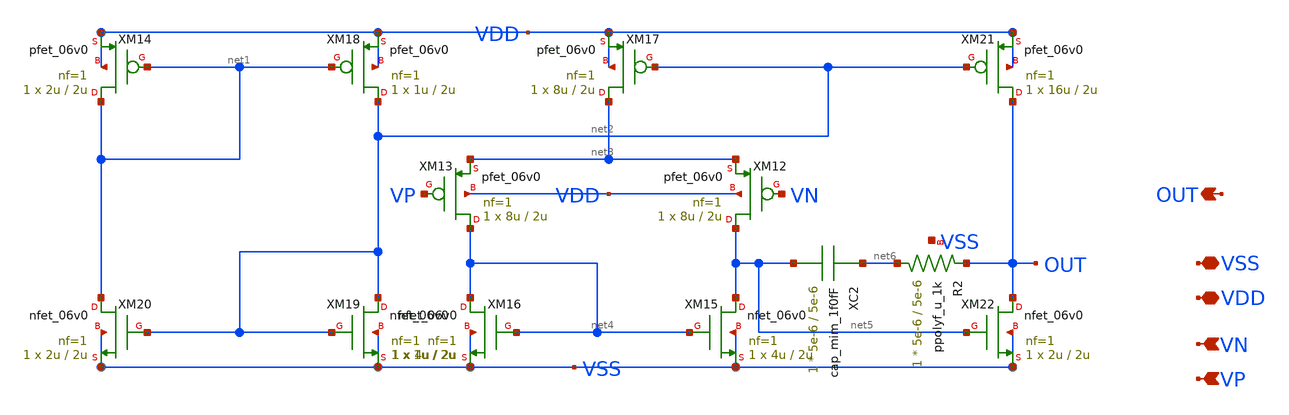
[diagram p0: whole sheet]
** sch_path: designs/libs/core_p-ota/p-6v-ota/p-6v-ota.sch
**.subckt p-6v-ota VN VP OUT VDD VSS
*.ipin VN
*.ipin VP
*.opin OUT
*.iopin VDD
*.iopin VSS
XM12 net5 VN net3 VDD pfet_06v0 L=2u W=8u nf=1 ad='int((nf+1)/2) * W/nf * 0.18u' as='int((nf+2)/2) * W/nf * 0.18u'
+ pd='2*int((nf+1)/2) * (W/nf + 0.18u)' ps='2*int((nf+2)/2) * (W/nf + 0.18u)' nrd='0.18u / W' nrs='0.18u / W'
+ sa=0 sb=0 sd=0 m=1
XM13 net4 VP net3 VDD pfet_06v0 L=2u W=8u nf=1 ad='int((nf+1)/2) * W/nf * 0.18u' as='int((nf+2)/2) * W/nf * 0.18u'
+ pd='2*int((nf+1)/2) * (W/nf + 0.18u)' ps='2*int((nf+2)/2) * (W/nf + 0.18u)' nrd='0.18u / W' nrs='0.18u / W'
+ sa=0 sb=0 sd=0 m=1
XM15 net5 net4 VSS VSS nfet_06v0 L=2u W=4u nf=1 ad='int((nf+1)/2) * W/nf * 0.18u' as='int((nf+2)/2) * W/nf * 0.18u'
+ pd='2*int((nf+1)/2) * (W/nf + 0.18u)' ps='2*int((nf+2)/2) * (W/nf + 0.18u)' nrd='0.18u / W' nrs='0.18u / W'
+ sa=0 sb=0 sd=0 m=1
XM16 net4 net4 VSS VSS nfet_06v0 L=2u W=4u nf=1 ad='int((nf+1)/2) * W/nf * 0.18u' as='int((nf+2)/2) * W/nf * 0.18u'
+ pd='2*int((nf+1)/2) * (W/nf + 0.18u)' ps='2*int((nf+2)/2) * (W/nf + 0.18u)' nrd='0.18u / W' nrs='0.18u / W'
+ sa=0 sb=0 sd=0 m=1
XM17 net3 net2 VDD VDD pfet_06v0 L=2u W=8u nf=1 ad='int((nf+1)/2) * W/nf * 0.18u' as='int((nf+2)/2) * W/nf * 0.18u'
+ pd='2*int((nf+1)/2) * (W/nf + 0.18u)' ps='2*int((nf+2)/2) * (W/nf + 0.18u)' nrd='0.18u / W' nrs='0.18u / W'
+ sa=0 sb=0 sd=0 m=1
XM14 net1 net1 VDD VDD pfet_06v0 L=2u W=2u nf=1 ad='int((nf+1)/2) * W/nf * 0.18u' as='int((nf+2)/2) * W/nf * 0.18u'
+ pd='2*int((nf+1)/2) * (W/nf + 0.18u)' ps='2*int((nf+2)/2) * (W/nf + 0.18u)' nrd='0.18u / W' nrs='0.18u / W'
+ sa=0 sb=0 sd=0 m=1
XM18 net2 net1 VDD VDD pfet_06v0 L=2u W=1u nf=1 ad='int((nf+1)/2) * W/nf * 0.18u' as='int((nf+2)/2) * W/nf * 0.18u'
+ pd='2*int((nf+1)/2) * (W/nf + 0.18u)' ps='2*int((nf+2)/2) * (W/nf + 0.18u)' nrd='0.18u / W' nrs='0.18u / W'
+ sa=0 sb=0 sd=0 m=1
XM19 net2 net2 VSS VSS nfet_06v0 L=2u W=1u nf=1 ad='int((nf+1)/2) * W/nf * 0.18u' as='int((nf+2)/2) * W/nf * 0.18u'
+ pd='2*int((nf+1)/2) * (W/nf + 0.18u)' ps='2*int((nf+2)/2) * (W/nf + 0.18u)' nrd='0.18u / W' nrs='0.18u / W'
+ sa=0 sb=0 sd=0 m=1
XM20 net1 net2 VSS VSS nfet_06v0 L=2u W=2u nf=1 ad='int((nf+1)/2) * W/nf * 0.18u' as='int((nf+2)/2) * W/nf * 0.18u'
+ pd='2*int((nf+1)/2) * (W/nf + 0.18u)' ps='2*int((nf+2)/2) * (W/nf + 0.18u)' nrd='0.18u / W' nrs='0.18u / W'
+ sa=0 sb=0 sd=0 m=1
XM21 OUT net2 VDD VDD pfet_06v0 L=2u W=16u nf=1 ad='int((nf+1)/2) * W/nf * 0.18u' as='int((nf+2)/2) * W/nf * 0.18u'
+ pd='2*int((nf+1)/2) * (W/nf + 0.18u)' ps='2*int((nf+2)/2) * (W/nf + 0.18u)' nrd='0.18u / W' nrs='0.18u / W'
+ sa=0 sb=0 sd=0 m=1
XM22 OUT net5 VSS VSS nfet_06v0 L=2u W=2u nf=1 ad='int((nf+1)/2) * W/nf * 0.18u' as='int((nf+2)/2) * W/nf * 0.18u'
+ pd='2*int((nf+1)/2) * (W/nf + 0.18u)' ps='2*int((nf+2)/2) * (W/nf + 0.18u)' nrd='0.18u / W' nrs='0.18u / W'
+ sa=0 sb=0 sd=0 m=1
XC2 net6 net5 cap_mim_1f0fF c_width=5e-6 c_length=5e-6 m=1
XR2 net6 OUT VSS ppolyf_u_1k r_width=5e-6 r_length=5e-6 m=1
**.ends
.end
